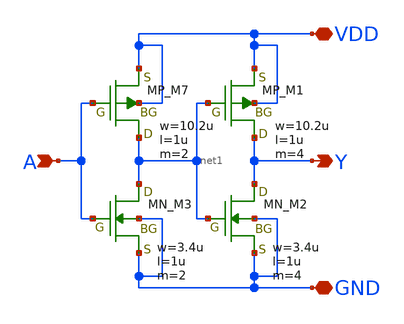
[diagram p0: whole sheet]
** sch_path: libs.tech/xschem/TR-1um_stdcell/BUF_X4.sch
**.subckt BUF_X4 A Y VDD GND
*.ipin A
*.opin Y
*.iopin VDD
*.iopin GND
XM7 net1 A VDD VDD PMOS w=10.2u l=1u nrd=0 nrs=0 m=2
XM1 Y net1 VDD VDD PMOS w=10.2u l=1u nrd=0 nrs=0 m=4
XM3 net1 A GND GND NMOS w=3.4u l=1u nrd=0 nrs=0 m=2
XM2 Y net1 GND GND NMOS w=3.4u l=1u nrd=0 nrs=0 m=4
**.ends
.end
